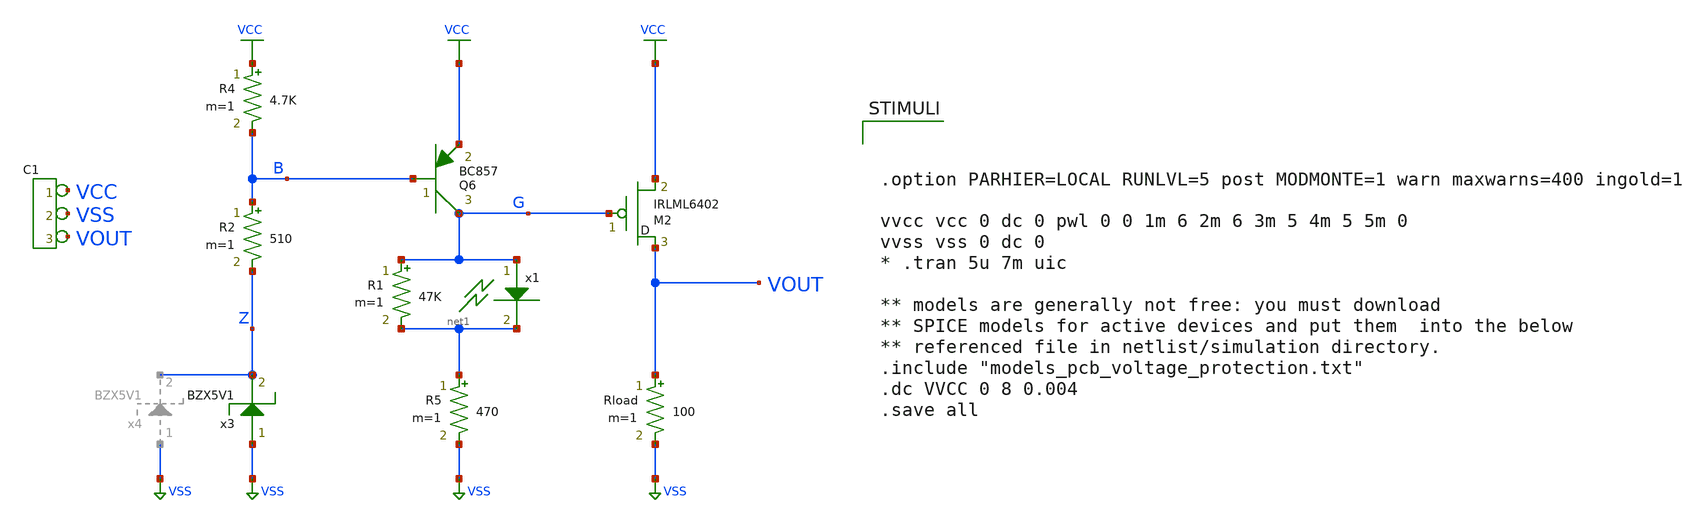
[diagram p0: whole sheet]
** sch_path: xschem_libs_newsym/pcb/pcb_voltage_protection/schematic/pcb_voltage_protection.sch
* Copyright (C) 1998-2024 Stefan Frederik Schippers
* This program is free software; you can redistribute it and/or modify
* it under the terms of the GNU General Public License as published by
* the Free Software Foundation; either version 2 of the License, or
* (at your option) any later version.
* This program is distributed in the hope that it will be useful,
* but WITHOUT ANY WARRANTY; without even the implied warranty of
* MERCHANTABILITY or FITNESS FOR A PARTICULAR PURPOSE.  See the
* GNU General Public License for more details.
* You should have received a copy of the GNU General Public License
* along with this program; if not, write to the Free Software
**.subckt pcb_voltage_protection
*connector(3,1) ?1 VCC ?1 VSS ?1 VOUT
Rload VOUT VSS 100 m=1
Q6 G B VCC BC857 area=1 m=1
x3 VSS Z BZX5V1
R4 VCC B 4.7K m=1
R5 net1 VSS 470 m=1
R2 B Z 510 m=1
XM2 VOUT G VCC IRLML6402 m=1
x1 G net1 D1N5765
R1 G net1 47K m=1
**** begin user architecture code



.option PARHIER=LOCAL RUNLVL=5 post MODMONTE=1 warn maxwarns=400 ingold=1

vvcc vcc 0 dc 0 pwl 0 0 1m 6 2m 6 3m 5 4m 5 5m 0
vvss vss 0 dc 0
* .tran 5u 7m uic

** models are generally not free: you must download
** SPICE models for active devices and put them  into the below
** referenced file in netlist/simulation directory.
.include "models_pcb_voltage_protection.txt"
.dc VVCC 0 8 0.004
.save all


**** end user architecture code
**.ends
.GLOBAL VCC
.GLOBAL VSS
.end
